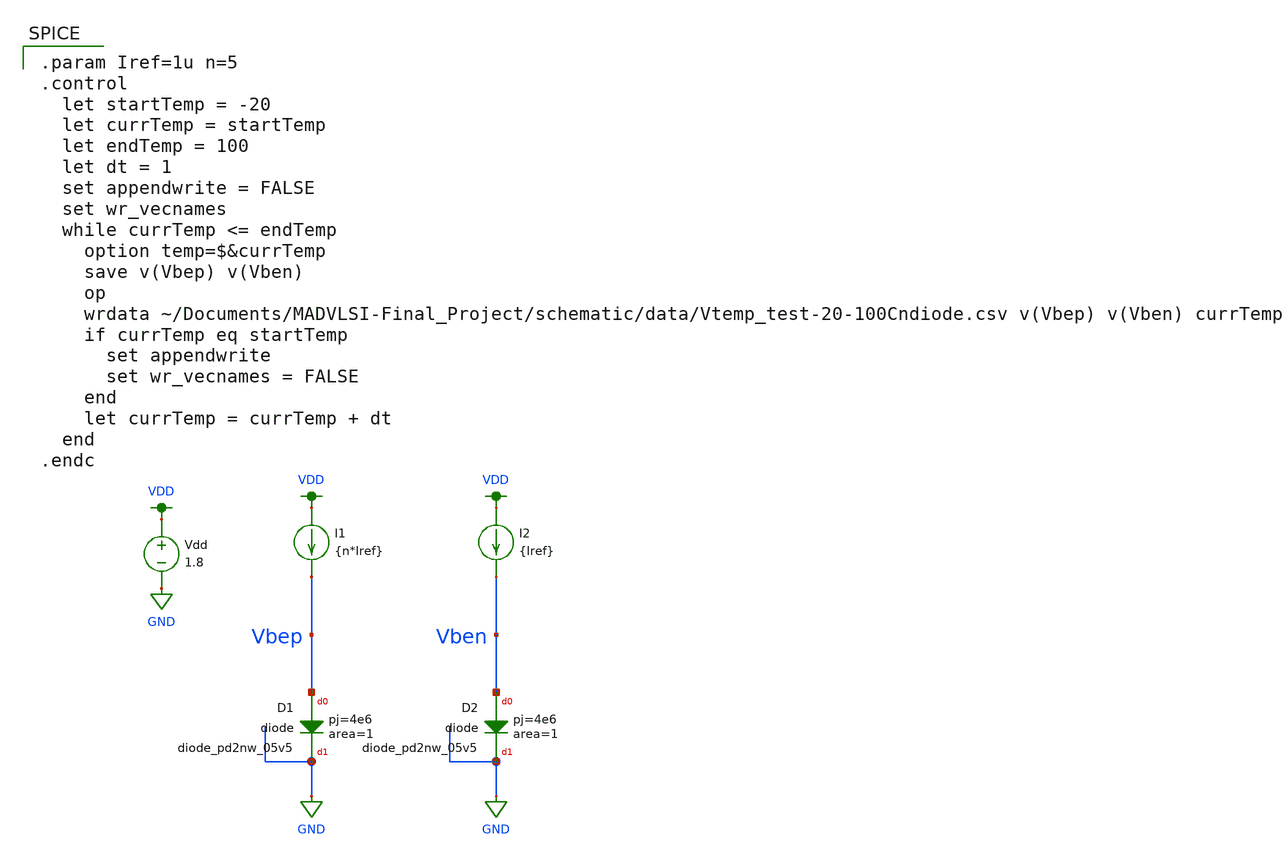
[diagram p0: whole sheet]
** sch_path: schematic/test/Vtemp_test.sch
**.subckt Vtemp_test
I1 VDD Vbep {n*Iref}
I2 VDD Vben {Iref}
Vdd VDD GND 1.8
XD1 Vbep GND sky130_fd_pr__diode_pd2nw_05v5 area=1 pj=4e6
XD2 Vben GND sky130_fd_pr__diode_pd2nw_05v5 area=1 pj=4e6
**** begin user architecture code

.option wnflag=1
.param MC_SWITCH=0.0
.lib ~/skywater/skywater-pdk/libraries/sky130_fd_pr_ngspice/latest/models/sky130.lib.spice tt


.param Iref=1u n=5
.control
  let startTemp = -20
  let currTemp = startTemp
  let endTemp = 100
  let dt = 1
  set appendwrite = FALSE
  set wr_vecnames
  while currTemp <= endTemp
    option temp=$&currTemp
    save v(Vbep) v(Vben)
    op
    wrdata ~/Documents/MADVLSI-Final_Project/schematic/data/Vtemp_test-20-100Cndiode.csv v(Vbep)
+ v(Vben) currTemp
    if currTemp eq startTemp
      set appendwrite
      set wr_vecnames = FALSE
    end
    let currTemp = currTemp + dt
  end
.endc

**** end user architecture code
**.ends
.GLOBAL GND
.GLOBAL VDD
.end
